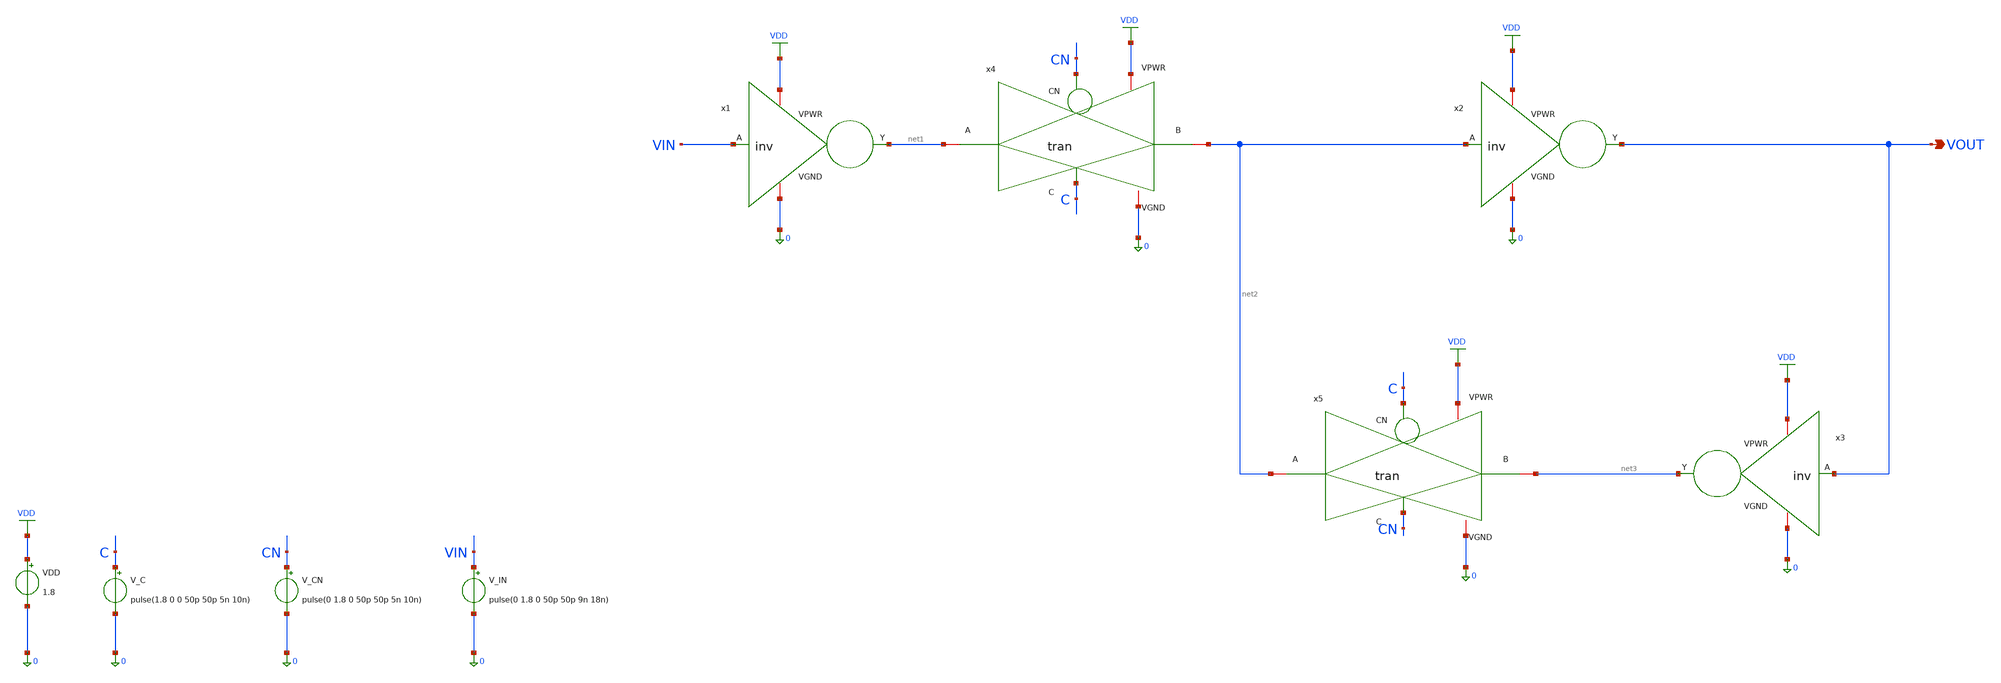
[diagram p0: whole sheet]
** sch_path: latch/latch_tb.sch
**.subckt latch_tb VOUT
*.opin VOUT
x1 VDD VIN net1 0 inv
x2 VDD net2 VOUT 0 inv
x3 VDD VOUT net3 0 inv
x4 CN VDD net2 net1 0 C tran
x5 C VDD net3 net2 0 CN tran
VDD VDD 0 1.8
V_C C 0 pulse(1.8 0 0 50p 50p 5n 10n)
V_CN CN 0 pulse(0 1.8 0 50p 50p 5n 10n)
V_IN VIN 0 pulse(0 1.8 0 50p 50p 9n 18n)
**** begin user architecture code

** opencircuitdesign pdks install
.lib $::SKYWATER_MODELS/sky130.lib.spice tt



.tran 0.00001n 11n
.control
  save all
    run
	meas tran delay TRIG v(C) VAL=0.9 RISE=1 TARG v(vout) VAL=0.9 RISE=1
	write /home/sushanth/.xschem/simulations/output.raw
  end
.endc


**** end user architecture code
**.ends
.GLOBAL VDD
.end
